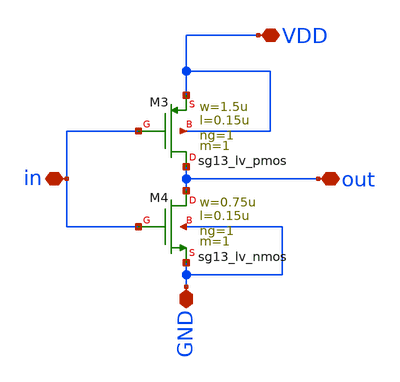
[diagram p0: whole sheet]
** sch_path: design/blocks/inverter/schematic/inverter.sch
**.subckt inverter VDD in out GND
*.iopin VDD
*.iopin in
*.iopin out
*.iopin GND
XM3 out in VDD VDD sg13_lv_pmos w=1.5u l=0.15u ng=1 m=1 mm_ok=1
XM4 out in GND GND sg13_lv_nmos w=0.75u l=0.15u ng=1 m=1 mm_ok=1
**.ends
.end
